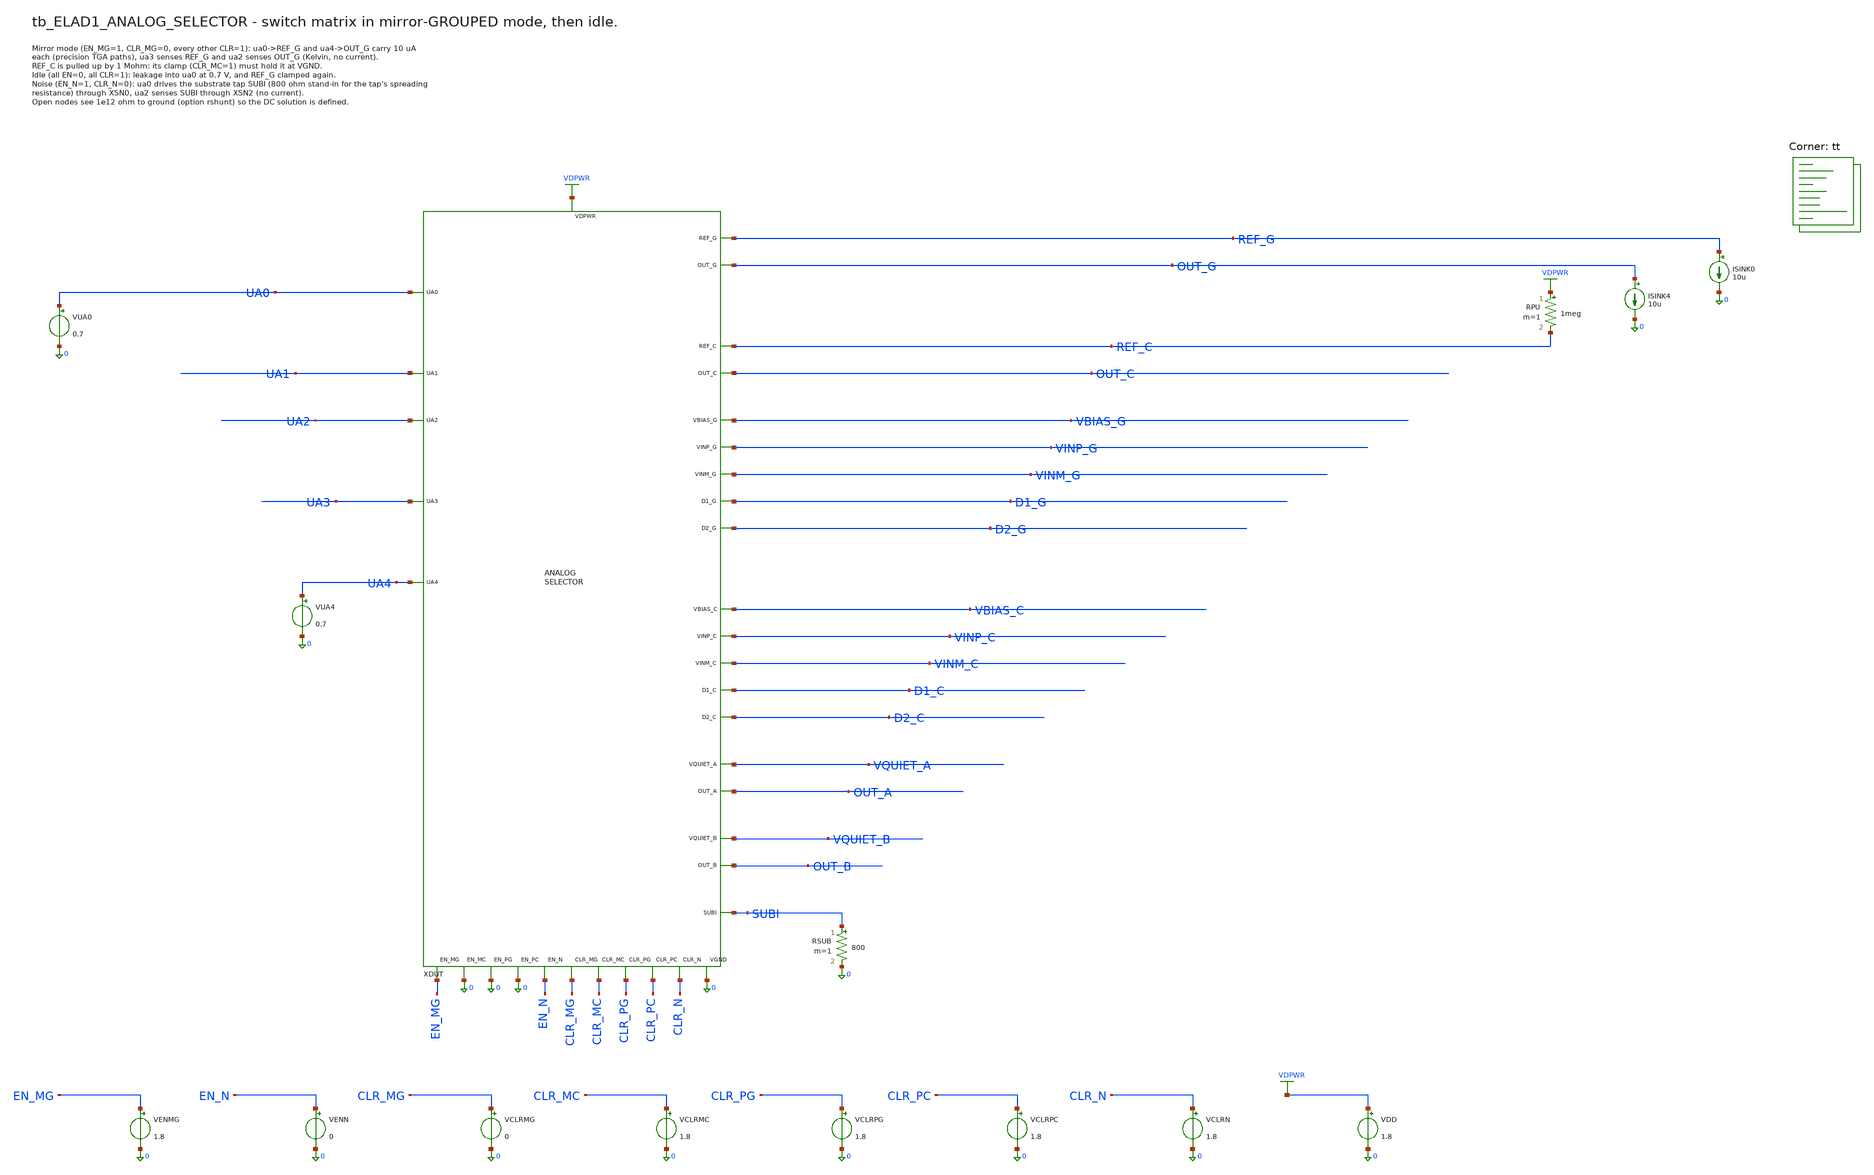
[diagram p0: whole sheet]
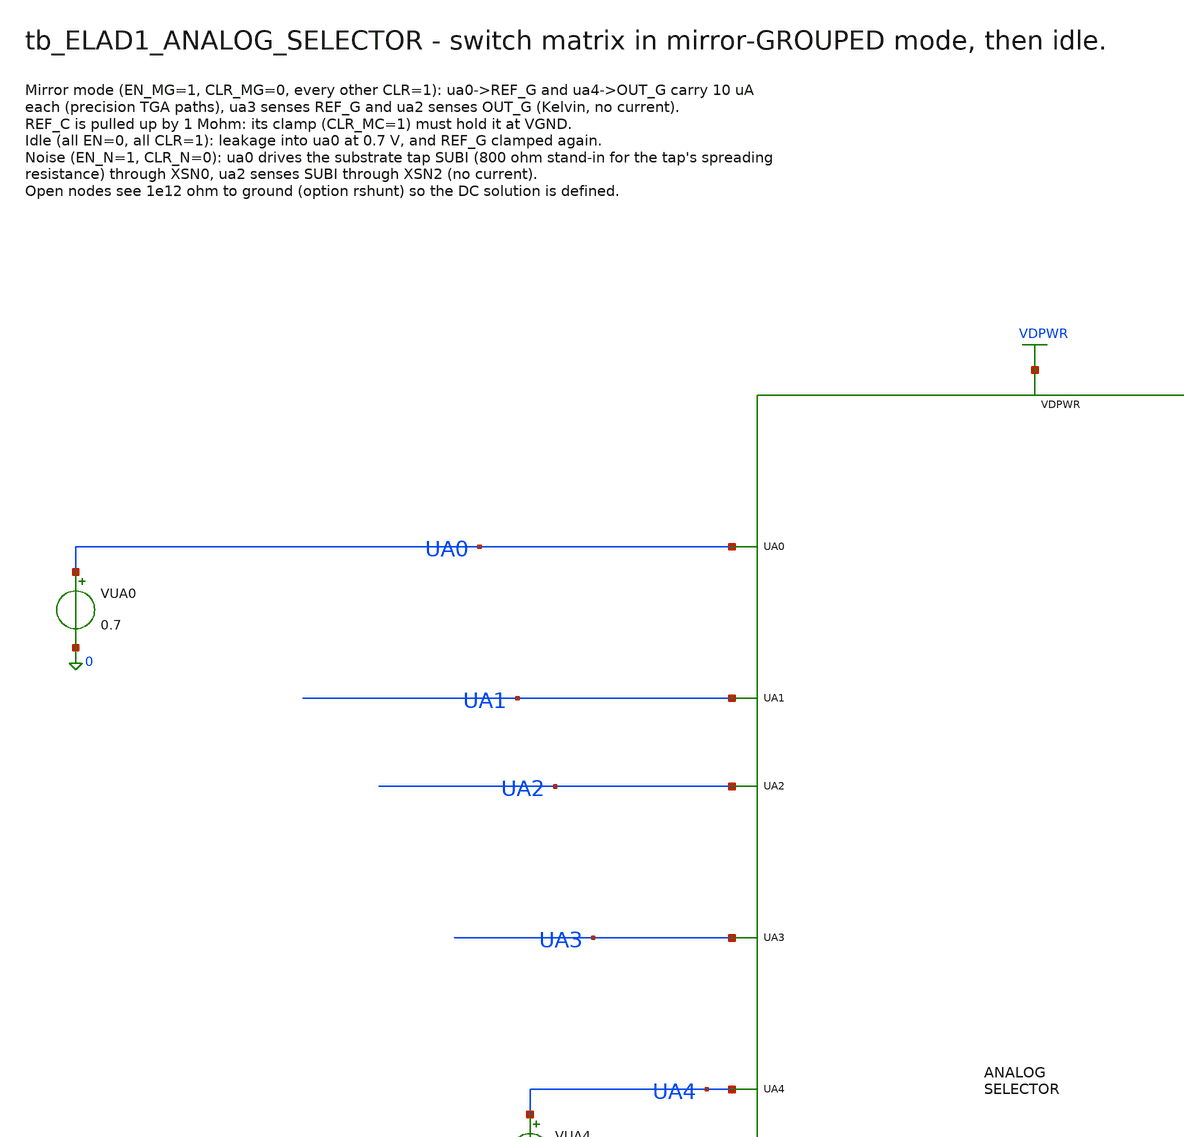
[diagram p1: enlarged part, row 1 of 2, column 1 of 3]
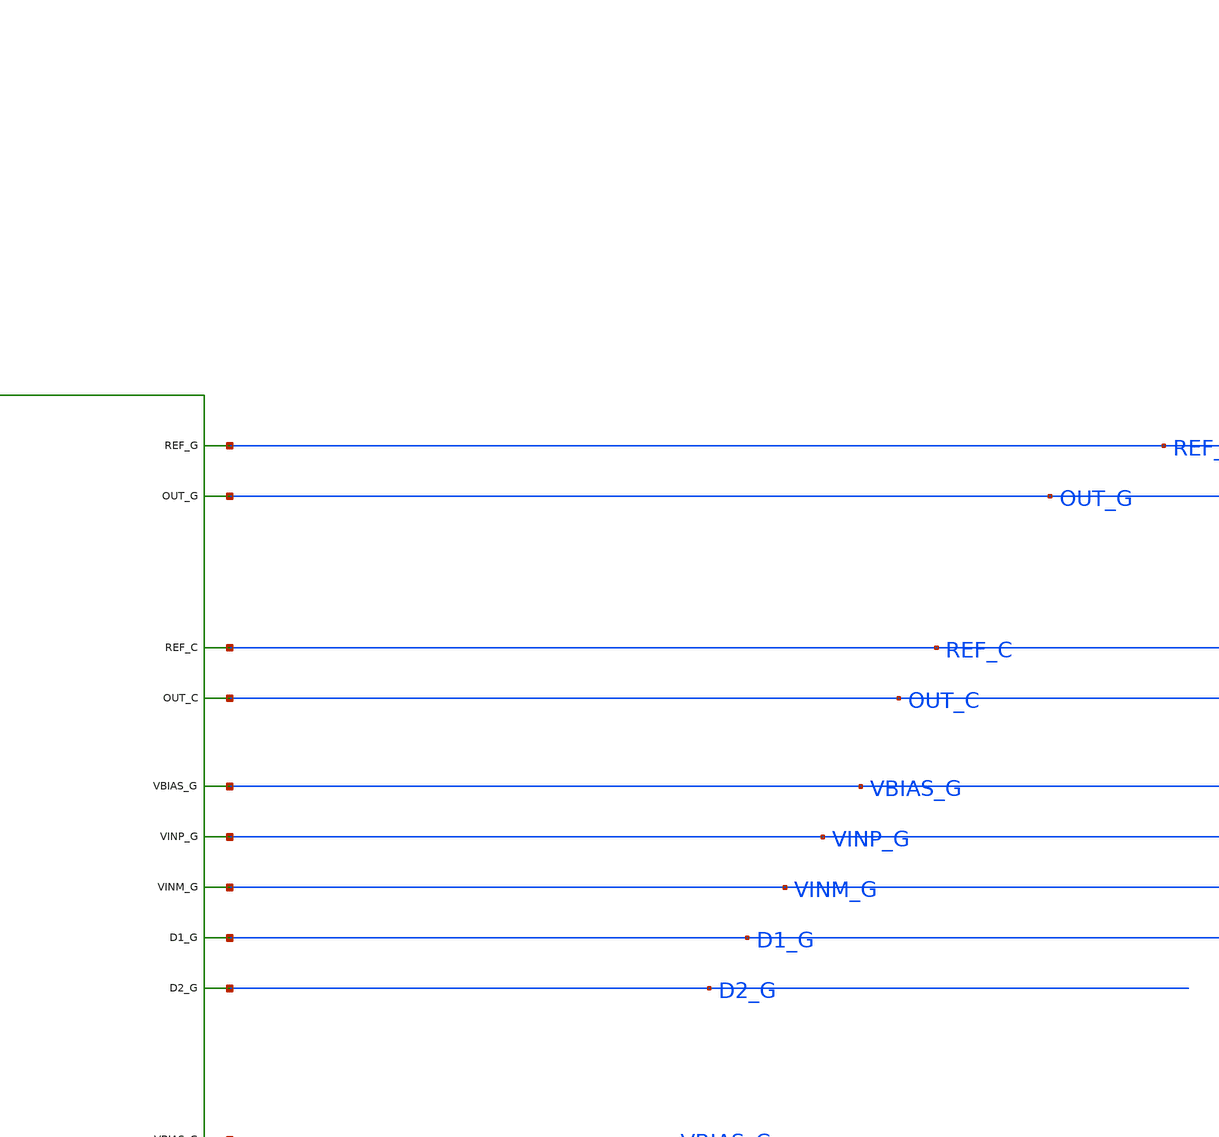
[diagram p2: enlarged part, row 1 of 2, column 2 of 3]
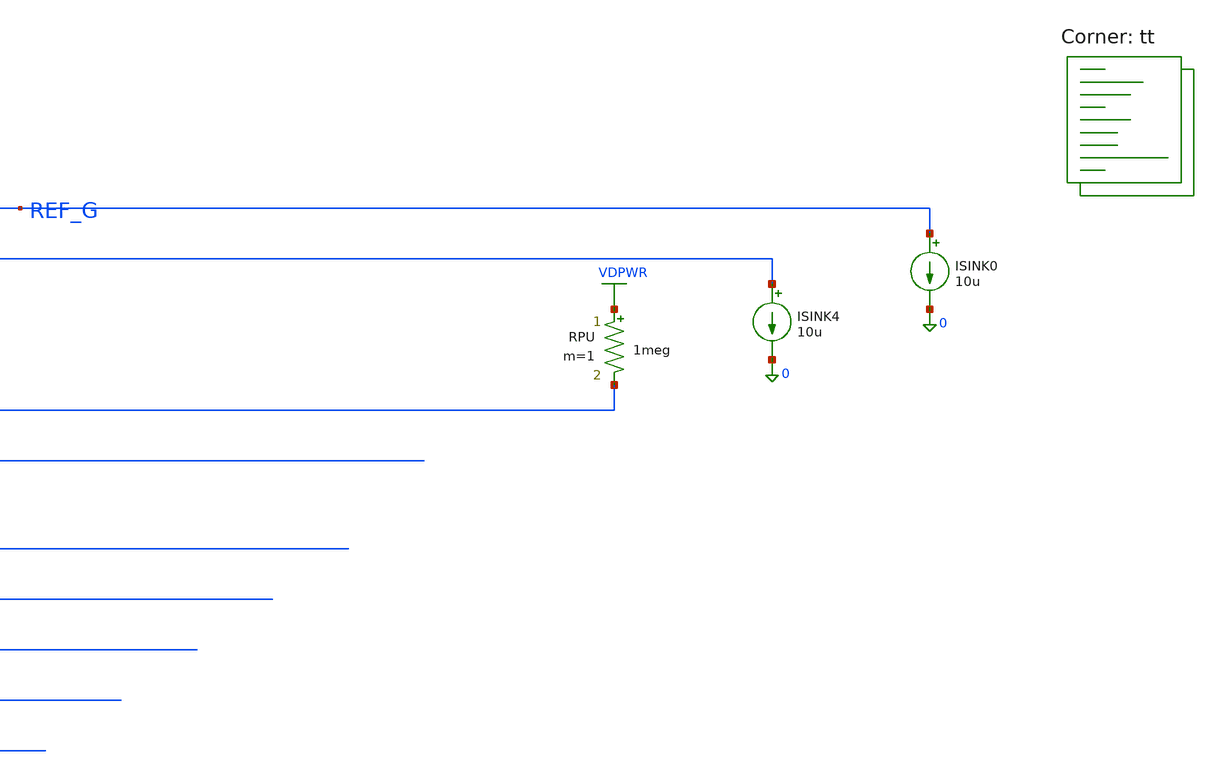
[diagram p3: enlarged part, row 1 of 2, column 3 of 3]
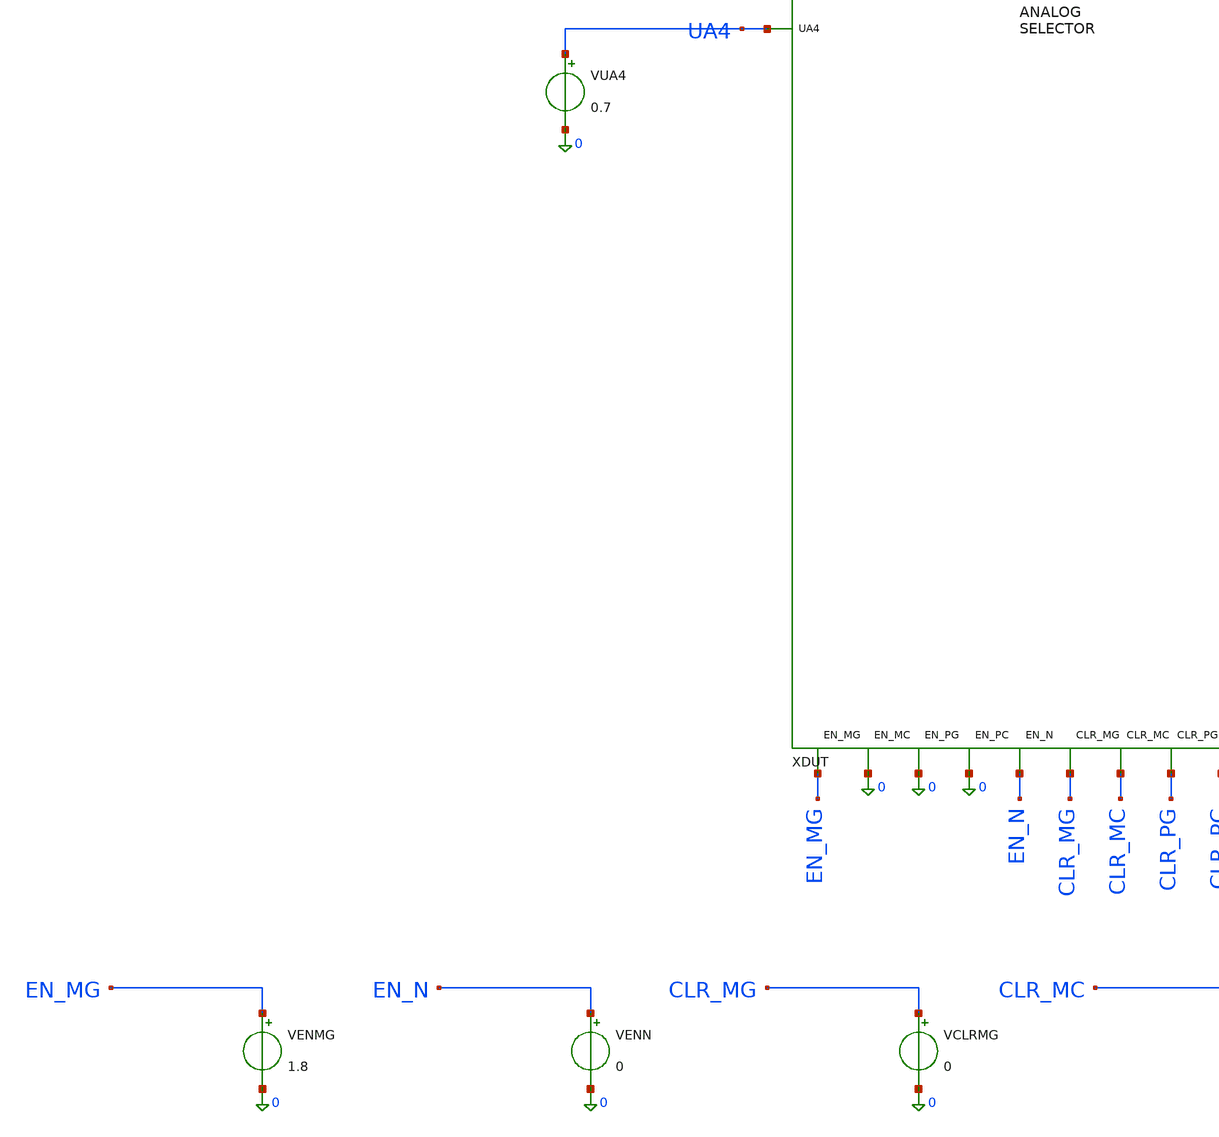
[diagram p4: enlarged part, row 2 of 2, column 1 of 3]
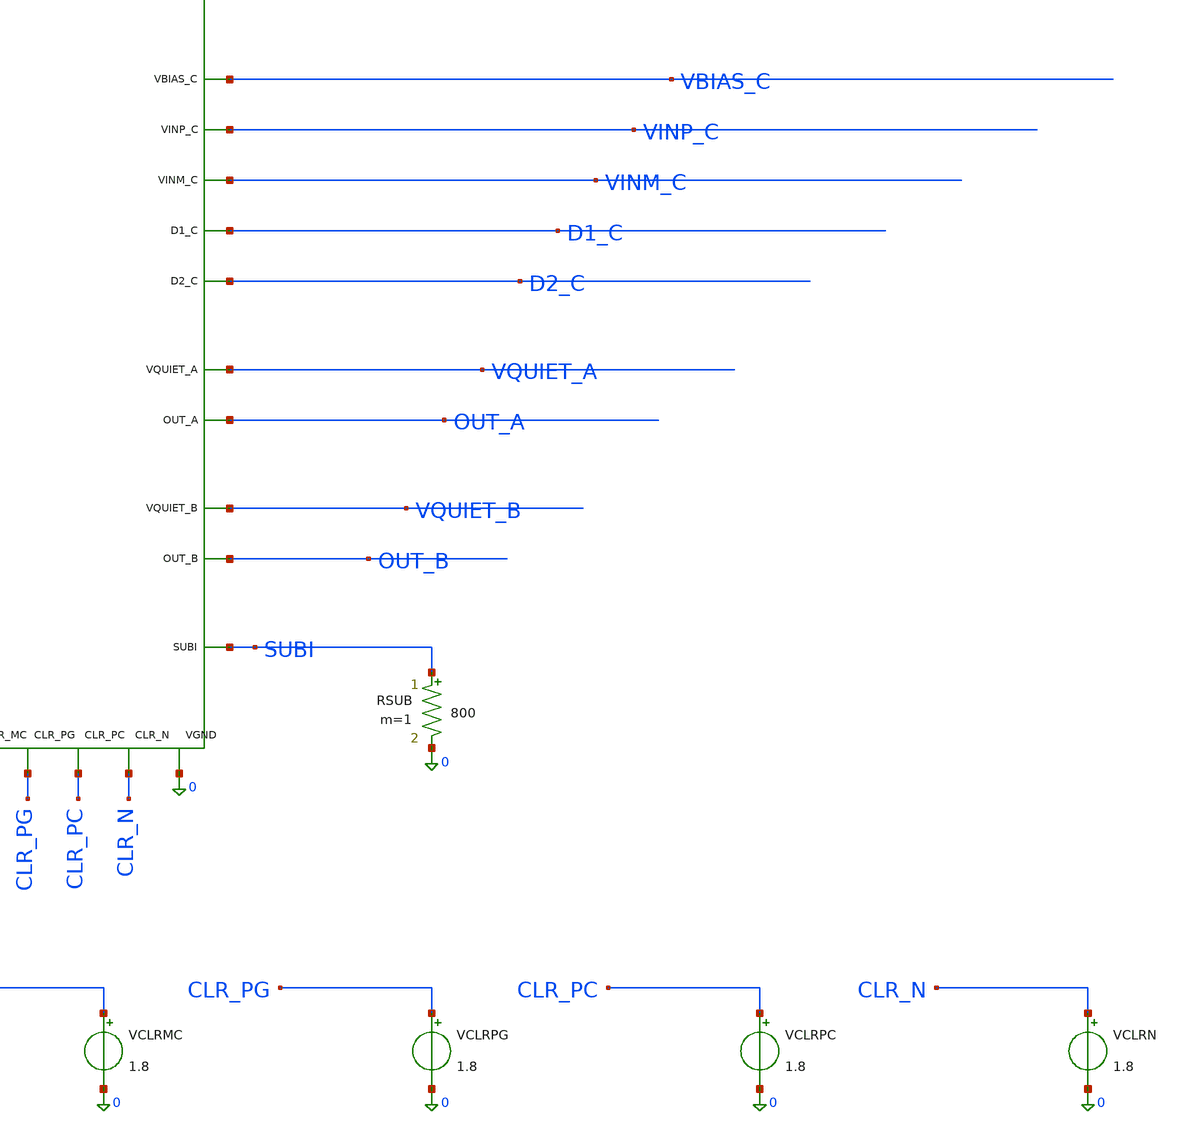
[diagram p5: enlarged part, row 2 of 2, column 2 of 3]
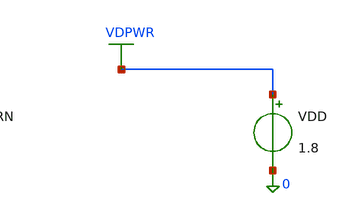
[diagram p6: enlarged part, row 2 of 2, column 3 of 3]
** sch_path: cells/ELAD1_ANALOG_SELECTOR/schematic/tb_ELAD1_ANALOG_SELECTOR.sch
**.subckt tb_ELAD1_ANALOG_SELECTOR
XDUT UA0 UA1 UA2 UA3 UA4 REF_G OUT_G REF_C OUT_C VBIAS_G VINP_G VINM_G D1_G D2_G VBIAS_C VINP_C
+ VINM_C D1_C D2_C VQUIET_A VQUIET_B OUT_A OUT_B SUBI EN_MG 0 0 0 EN_N CLR_MG CLR_MC CLR_PG CLR_PC CLR_N
+ VDPWR 0 ELAD1_ANALOG_SELECTOR
VUA4 UA4 0 0.7
VUA0 UA0 0 0.7
RSUB SUBI 0 800 m=1
RPU VDPWR REF_C 1meg m=1
ISINK4 OUT_G 0 10u
ISINK0 REF_G 0 10u
VENMG EN_MG 0 1.8
VENN EN_N 0 0
VCLRMG CLR_MG 0 0
VCLRMC CLR_MC 0 1.8
VCLRPG CLR_PG 0 1.8
VCLRPC CLR_PC 0 1.8
VCLRN CLR_N 0 1.8
VDD VDPWR 0 1.8
**** begin user architecture code

.control
option rshunt=1e12
op
let ron_ua0 = (v(UA0)-v(REF_G))/10e-6
let ron_ua4 = (v(UA4)-v(OUT_G))/10e-6
let sense_err_ua3 = abs(v(UA3)-v(REF_G))
let sense_err_ua2 = abs(v(UA2)-v(OUT_G))
let v_ref_c_clamped = v(REF_C)
print ron_ua0 ron_ua4 sense_err_ua3 sense_err_ua2 v_ref_c_clamped
alter VENMG dc = 0
alter VCLRMG dc = 1.8
alter ISINK0 dc = 0
alter ISINK4 dc = 0
op
let i_idle_ua0 = abs(i(VUA0))
let v_ref_g_idle = abs(v(REF_G))
print i_idle_ua0 v_ref_g_idle
alter VENN dc = 1.8
alter VCLRN dc = 0
alter VUA0 dc = 0.1
op
let ron_subi = (v(UA0)-v(SUBI))/abs(i(VUA0))
let sense_err_subi = abs(v(UA2)-v(SUBI))
let v_subi = v(SUBI)
print ron_subi sense_err_subi v_subi
write tb_ELAD1_ANALOG_SELECTOR.raw
.endc

.lib $::SKYWATER_MODELS/sky130.lib.spice tt
**** end user architecture code
**.ends

* expanding   symbol:  ELAD1_ANALOG_SELECTOR.sym # of pins=36
** sym_path: cells/ELAD1_ANALOG_SELECTOR/schematic/ELAD1_ANALOG_SELECTOR.sym
** sch_path: cells/ELAD1_ANALOG_SELECTOR/schematic/ELAD1_ANALOG_SELECTOR.sch
.subckt ELAD1_ANALOG_SELECTOR UA0 UA1 UA2 UA3 UA4 REF_G OUT_G REF_C OUT_C VBIAS_G VINP_G VINM_G D1_G
+ D2_G VBIAS_C VINP_C VINM_C D1_C D2_C VQUIET_A VQUIET_B OUT_A OUT_B SUBI EN_MG EN_MC EN_PG EN_PC EN_N
+ CLR_MG CLR_MC CLR_PG CLR_PC CLR_N VDPWR VGND
*.iopin UA0
*.iopin UA1
*.iopin UA2
*.iopin UA3
*.iopin UA4
*.iopin REF_G
*.iopin OUT_G
*.iopin REF_C
*.iopin OUT_C
*.iopin VBIAS_G
*.iopin VINP_G
*.iopin VINM_G
*.iopin D1_G
*.iopin D2_G
*.iopin VBIAS_C
*.iopin VINP_C
*.iopin VINM_C
*.iopin D1_C
*.iopin D2_C
*.iopin VQUIET_A
*.iopin VQUIET_B
*.iopin OUT_A
*.iopin OUT_B
*.iopin SUBI
*.iopin EN_MG
*.iopin EN_MC
*.iopin EN_PG
*.iopin EN_PC
*.iopin EN_N
*.iopin CLR_MG
*.iopin CLR_MC
*.iopin CLR_PG
*.iopin CLR_PC
*.iopin CLR_N
*.iopin VDPWR
*.iopin VGND
XSMG0 UA0 REF_G EN_MG ENB_MG VDPWR VGND ELAD1_TGA
XSMG3 UA3 REF_G EN_MG ENB_MG VDPWR VGND ELAD1_TGB
XSMG2 UA2 OUT_G EN_MG ENB_MG VDPWR VGND ELAD1_TGB
XSMG4 UA4 OUT_G EN_MG ENB_MG VDPWR VGND ELAD1_TGA
XCL_REF_G REF_G CLR_MG VGND ELAD1_CLAMP
XSMC0 UA0 REF_C EN_MC ENB_MC VDPWR VGND ELAD1_TGA
XSMC3 UA3 REF_C EN_MC ENB_MC VDPWR VGND ELAD1_TGB
XSMC2 UA2 OUT_C EN_MC ENB_MC VDPWR VGND ELAD1_TGB
XSMC4 UA4 OUT_C EN_MC ENB_MC VDPWR VGND ELAD1_TGA
XCL_REF_C REF_C CLR_MC VGND ELAD1_CLAMP
XSPG0 UA0 VBIAS_G EN_PG ENB_PG VDPWR VGND ELAD1_TGA
XSPG1 UA1 VINP_G EN_PG ENB_PG VDPWR VGND ELAD1_TGB
XSPG2 UA2 VINM_G EN_PG ENB_PG VDPWR VGND ELAD1_TGB
XSPG3 UA3 D1_G EN_PG ENB_PG VDPWR VGND ELAD1_TGA
XSPG4 UA4 D2_G EN_PG ENB_PG VDPWR VGND ELAD1_TGA
XCL_VBIAS_G VBIAS_G CLR_PG VGND ELAD1_CLAMP
XCL_VINP_G VINP_G CLR_PG VGND ELAD1_CLAMP
XCL_VINM_G VINM_G CLR_PG VGND ELAD1_CLAMP
XSPC0 UA0 VBIAS_C EN_PC ENB_PC VDPWR VGND ELAD1_TGA
XSPC1 UA1 VINP_C EN_PC ENB_PC VDPWR VGND ELAD1_TGB
XSPC2 UA2 VINM_C EN_PC ENB_PC VDPWR VGND ELAD1_TGB
XSPC3 UA3 D1_C EN_PC ENB_PC VDPWR VGND ELAD1_TGA
XSPC4 UA4 D2_C EN_PC ENB_PC VDPWR VGND ELAD1_TGA
XCL_VBIAS_C VBIAS_C CLR_PC VGND ELAD1_CLAMP
XCL_VINP_C VINP_C CLR_PC VGND ELAD1_CLAMP
XCL_VINM_C VINM_C CLR_PC VGND ELAD1_CLAMP
XSN0 UA0 SUBI EN_N ENB_N VDPWR VGND ELAD1_TGB
XSN2 UA2 SUBI EN_N ENB_N VDPWR VGND ELAD1_TGB
XSN1A UA1 VQUIET_A EN_N ENB_N VDPWR VGND ELAD1_TGB
XSN3 UA3 OUT_A EN_N ENB_N VDPWR VGND ELAD1_TSW
XSN1B UA1 VQUIET_B EN_N ENB_N VDPWR VGND ELAD1_TGB
XSN4 UA4 OUT_B EN_N ENB_N VDPWR VGND ELAD1_TSW
XCL_VQ_A VQUIET_A CLR_N VGND ELAD1_CLAMP
XCL_VQ_B VQUIET_B CLR_N VGND ELAD1_CLAMP
XINV_MG EN_MG ENB_MG VDPWR VGND ELAD1_INV
XINV_MC EN_MC ENB_MC VDPWR VGND ELAD1_INV
XINV_PG EN_PG ENB_PG VDPWR VGND ELAD1_INV
XINV_PC EN_PC ENB_PC VDPWR VGND ELAD1_INV
XINV_N EN_N ENB_N VDPWR VGND ELAD1_INV
.ends


* expanding   symbol:  ELAD1_TGA.sym # of pins=6
** sym_path: cells/ELAD1_TGA/schematic/ELAD1_TGA.sym
** sch_path: cells/ELAD1_TGA/schematic/ELAD1_TGA.sch
.subckt ELAD1_TGA A B EN ENB VDPWR VGND
*.iopin A
*.iopin B
*.iopin EN
*.iopin ENB
*.iopin VDPWR
*.iopin VGND
XMN A EN B VGND sky130_fd_pr__nfet_01v8_lvt L=0.15 W=4 nf=1 ad='int((1 + 1)/2) * 4 / 1 * 0.29' as='int((1 + 2)/2) * 4 / 1 * 0.29'
+ pd='2*int((1 + 1)/2) * (4 / 1 + 0.29)' ps='2*int((1 + 2)/2) * (4 / 1 + 0.29)' nrd='0.29 / 4 ' nrs='0.29 / 4 '
+ sa=0 sb=0 sd=0 mult=1 m=1
XMP A ENB B VDPWR sky130_fd_pr__pfet_01v8_lvt L=0.35 W=12 nf=1 ad='int((1 + 1)/2) * 12 / 1 * 0.29' as='int((1 + 2)/2) * 12 / 1 * 0.29'
+ pd='2*int((1 + 1)/2) * (12 / 1 + 0.29)' ps='2*int((1 + 2)/2) * (12 / 1 + 0.29)' nrd='0.29 / 12 ' nrs='0.29 / 12 '
+ sa=0 sb=0 sd=0 mult=1 m=1
.ends


* expanding   symbol:  ELAD1_TGB.sym # of pins=6
** sym_path: cells/ELAD1_TGB/schematic/ELAD1_TGB.sym
** sch_path: cells/ELAD1_TGB/schematic/ELAD1_TGB.sch
.subckt ELAD1_TGB A B EN ENB VDPWR VGND
*.iopin A
*.iopin B
*.iopin EN
*.iopin ENB
*.iopin VDPWR
*.iopin VGND
XMN A EN B VGND sky130_fd_pr__nfet_01v8 L=0.15 W=1 nf=1 ad='int((1 + 1)/2) * 1 / 1 * 0.29' as='int((1 + 2)/2) * 1 / 1 * 0.29'
+ pd='2*int((1 + 1)/2) * (1 / 1 + 0.29)' ps='2*int((1 + 2)/2) * (1 / 1 + 0.29)' nrd='0.29 / 1 ' nrs='0.29 / 1 '
+ sa=0 sb=0 sd=0 mult=1 m=1
XMP A ENB B VDPWR sky130_fd_pr__pfet_01v8 L=0.15 W=2 nf=1 ad='int((nf+1)/2) * W/nf * 0.29' as='int((nf+2)/2) * W/nf * 0.29'
+ pd='2*int((nf+1)/2) * (W/nf + 0.29)' ps='2*int((nf+2)/2) * (W/nf + 0.29)' nrd='0.29 / W' nrs='0.29 / W'
+ sa=0 sb=0 sd=0 mult=1 m=1
.ends


* expanding   symbol:  ELAD1_CLAMP.sym # of pins=3
** sym_path: cells/ELAD1_CLAMP/schematic/ELAD1_CLAMP.sym
** sch_path: cells/ELAD1_CLAMP/schematic/ELAD1_CLAMP.sch
.subckt ELAD1_CLAMP NODE CLR VGND
*.iopin NODE
*.iopin CLR
*.iopin VGND
XM NODE CLR VGND VGND sky130_fd_pr__nfet_01v8 L=1 W=0.42 nf=1 ad='int((1 + 1)/2) * 0.42 / 1 * 0.29' as='int((1 + 2)/2) * 0.42 / 1 * 0.29'
+ pd='2*int((1 + 1)/2) * (0.42 / 1 + 0.29)' ps='2*int((1 + 2)/2) * (0.42 / 1 + 0.29)' nrd='0.29 / 0.42 '
+ nrs='0.29 / 0.42 ' sa=0 sb=0 sd=0 mult=1 m=1
.ends


* expanding   symbol:  ELAD1_TSW.sym # of pins=6
** sym_path: cells/ELAD1_TSW/schematic/ELAD1_TSW.sym
** sch_path: cells/ELAD1_TSW/schematic/ELAD1_TSW.sch
.subckt ELAD1_TSW A B EN ENB VDPWR VGND
*.iopin A
*.iopin B
*.iopin EN
*.iopin ENB
*.iopin VDPWR
*.iopin VGND
x1 A M EN ENB VDPWR VGND ELAD1_TGA
x1 M B EN ENB VDPWR VGND ELAD1_TGA
XMN1 M ENB VGND VGND sky130_fd_pr__nfet_01v8 L=0.15 W=1 nf=1 ad='int((1 + 1)/2) * 1 / 1 * 0.29' as='int((1 + 2)/2) * 1 / 1 * 0.29'
+ pd='2*int((1 + 1)/2) * (1 / 1 + 0.29)' ps='2*int((1 + 2)/2) * (1 / 1 + 0.29)' nrd='0.29 / 1 ' nrs='0.29 / 1 '
+ sa=0 sb=0 sd=0 mult=1 m=1
.ends


* expanding   symbol:  ELAD1_INV.sym # of pins=4
** sym_path: cells/ELAD1_INV/schematic/ELAD1_INV.sym
** sch_path: cells/ELAD1_INV/schematic/ELAD1_INV.sch
.subckt ELAD1_INV A Y VDPWR VGND
*.iopin A
*.iopin Y
*.iopin VDPWR
*.iopin VGND
XMN Y A VGND VGND sky130_fd_pr__nfet_01v8 L=0.15 W=0.65 nf=1 ad='int((1 + 1)/2) * 0.65 / 1 * 0.29' as='int((1 + 2)/2) * 0.65 / 1 * 0.29'
+ pd='2*int((1 + 1)/2) * (0.65 / 1 + 0.29)' ps='2*int((1 + 2)/2) * (0.65 / 1 + 0.29)' nrd='0.29 / 0.65 '
+ nrs='0.29 / 0.65 ' sa=0 sb=0 sd=0 mult=1 m=1
XMP Y A VDPWR VDPWR sky130_fd_pr__pfet_01v8 L=0.15 W=1 nf=1 ad='int((nf+1)/2) * W/nf * 0.29' as='int((nf+2)/2) * W/nf * 0.29'
+ pd='2*int((nf+1)/2) * (W/nf + 0.29)' ps='2*int((nf+2)/2) * (W/nf + 0.29)' nrd='0.29 / W' nrs='0.29 / W'
+ sa=0 sb=0 sd=0 mult=1 m=1
.ends

.GLOBAL VGND
.GLOBAL VDPWR
.end
